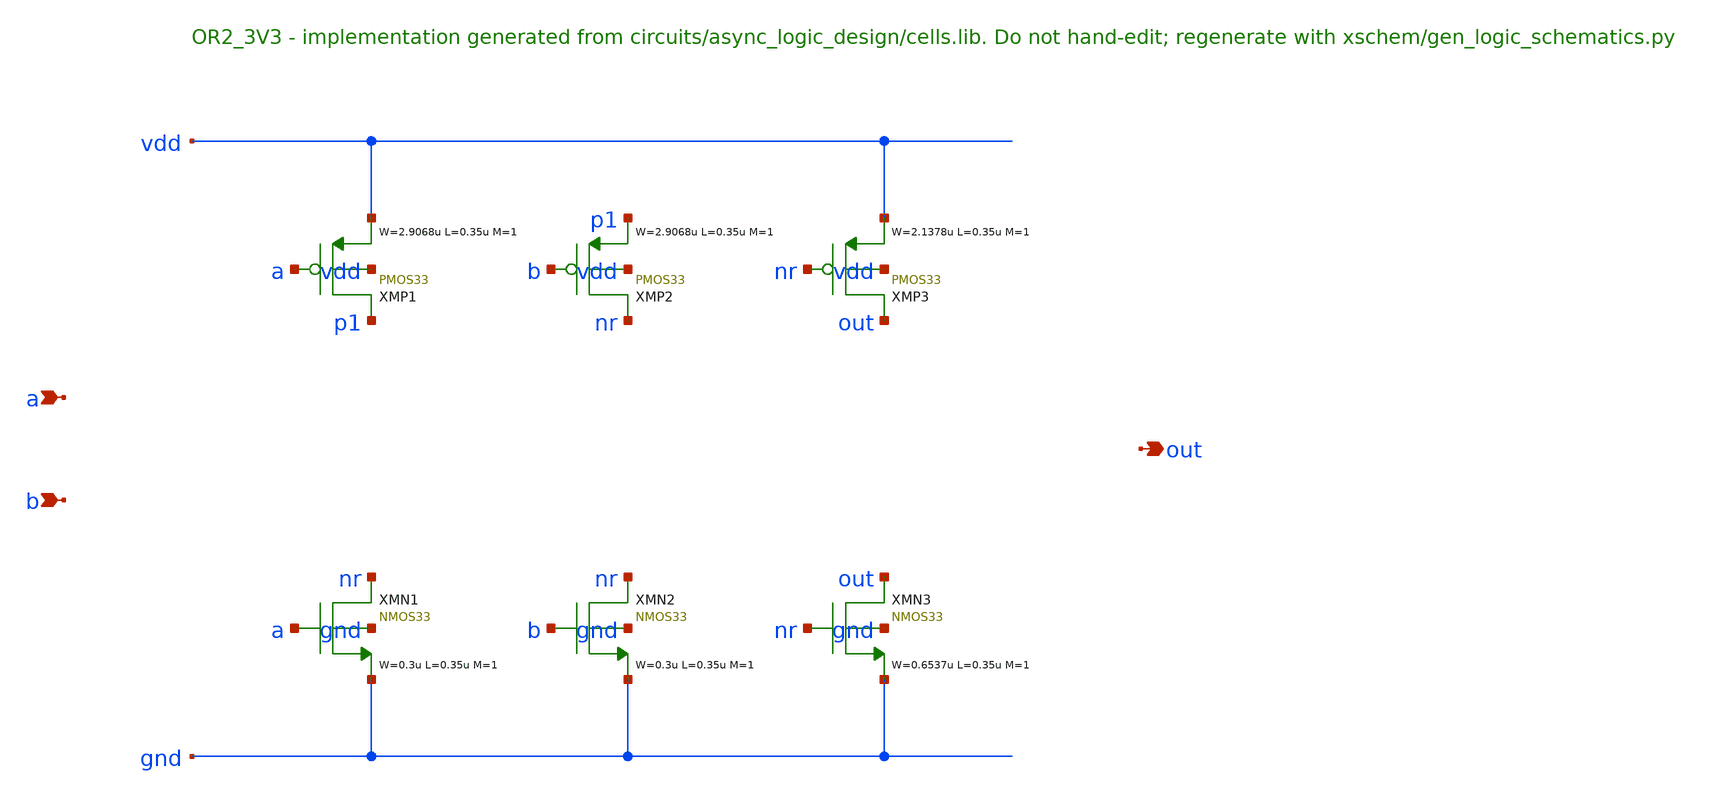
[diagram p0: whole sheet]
** sch_path: xschem/logic/OR2_3V3.sch
**.subckt OR2_3V3 a b out
*.ipin a
*.ipin b
*.opin out
XMP1 p1 a vdd vdd PMOS33 W=2.9068u L=0.35u M=1 MM_SIGMA=0
XMP2 nr b p1 vdd PMOS33 W=2.9068u L=0.35u M=1 MM_SIGMA=0
XMP3 out nr vdd vdd PMOS33 W=2.1378u L=0.35u M=1 MM_SIGMA=0
XMN1 nr a gnd gnd NMOS33 W=0.3u L=0.35u M=1 MM_SIGMA=0
XMN2 nr b gnd gnd NMOS33 W=0.3u L=0.35u M=1 MM_SIGMA=0
XMN3 out nr gnd gnd NMOS33 W=0.6537u L=0.35u M=1 MM_SIGMA=0
**.ends
.end
